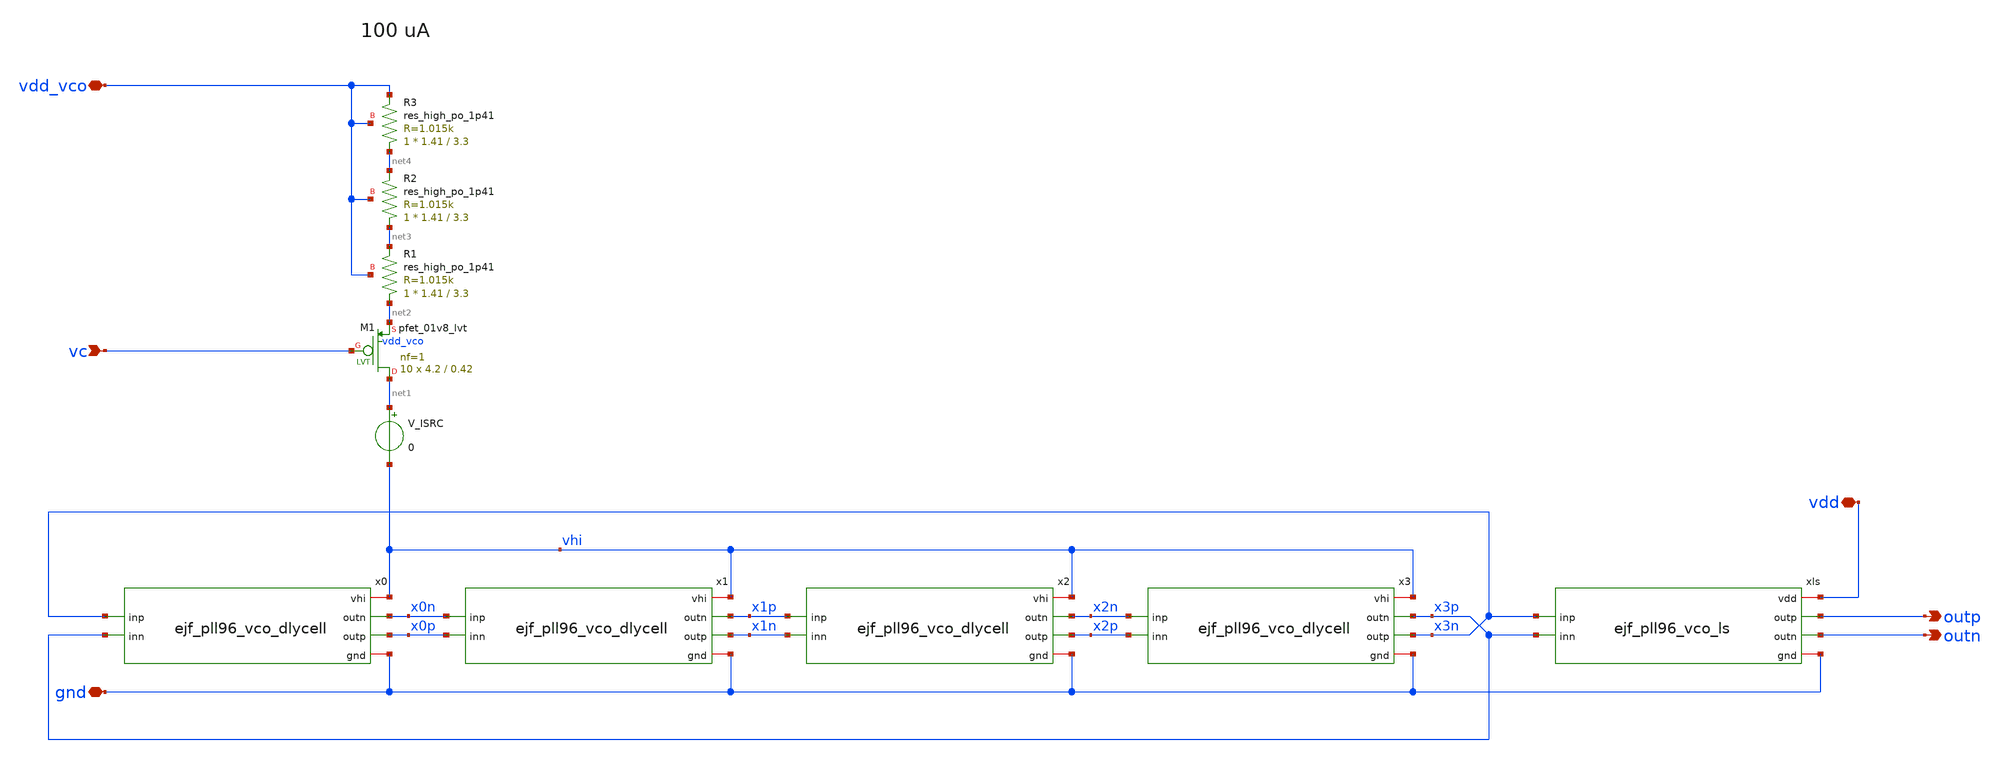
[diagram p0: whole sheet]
** sch_path: xschem/ejf_pll96_vco.sch
**.subckt ejf_pll96_vco vc vdd_vco outp gnd vdd outn
*.ipin vc
*.iopin vdd_vco
*.opin outp
*.iopin gnd
*.iopin vdd
*.opin outn
x1 vhi x1p x1n x0n x0p gnd ejf_pll96_vco_dlycell
x2 vhi x2n x2p x1p x1n gnd ejf_pll96_vco_dlycell
x0 vhi x0n x0p x3n x3p gnd ejf_pll96_vco_dlycell
x3 vhi x3p x3n x2n x2p gnd ejf_pll96_vco_dlycell
xls vdd x3n outp outn x3p gnd ejf_pll96_vco_ls
V_ISRC net1 vhi 0
XM1 net1 vc net2 vdd_vco sky130_fd_pr__pfet_01v8_lvt L=0.42 W=4.2 nf=1 ad='int((nf+1)/2) * W/nf * 0.29'
+ as='int((nf+2)/2) * W/nf * 0.29' pd='2*int((nf+1)/2) * (W/nf + 0.29)' ps='2*int((nf+2)/2) * (W/nf + 0.29)'
+ nrd='0.29 / W' nrs='0.29 / W' sa=0 sb=0 sd=0 mult=10 m=10
XR1 net2 net3 vdd_vco sky130_fd_pr__res_high_po_1p41 L=3.3 mult=1 m=1
XR2 net3 net4 vdd_vco sky130_fd_pr__res_high_po_1p41 L=3.3 mult=1 m=1
XR3 net4 vdd_vco vdd_vco sky130_fd_pr__res_high_po_1p41 L=3.3 mult=1 m=1
**.ends
.end
